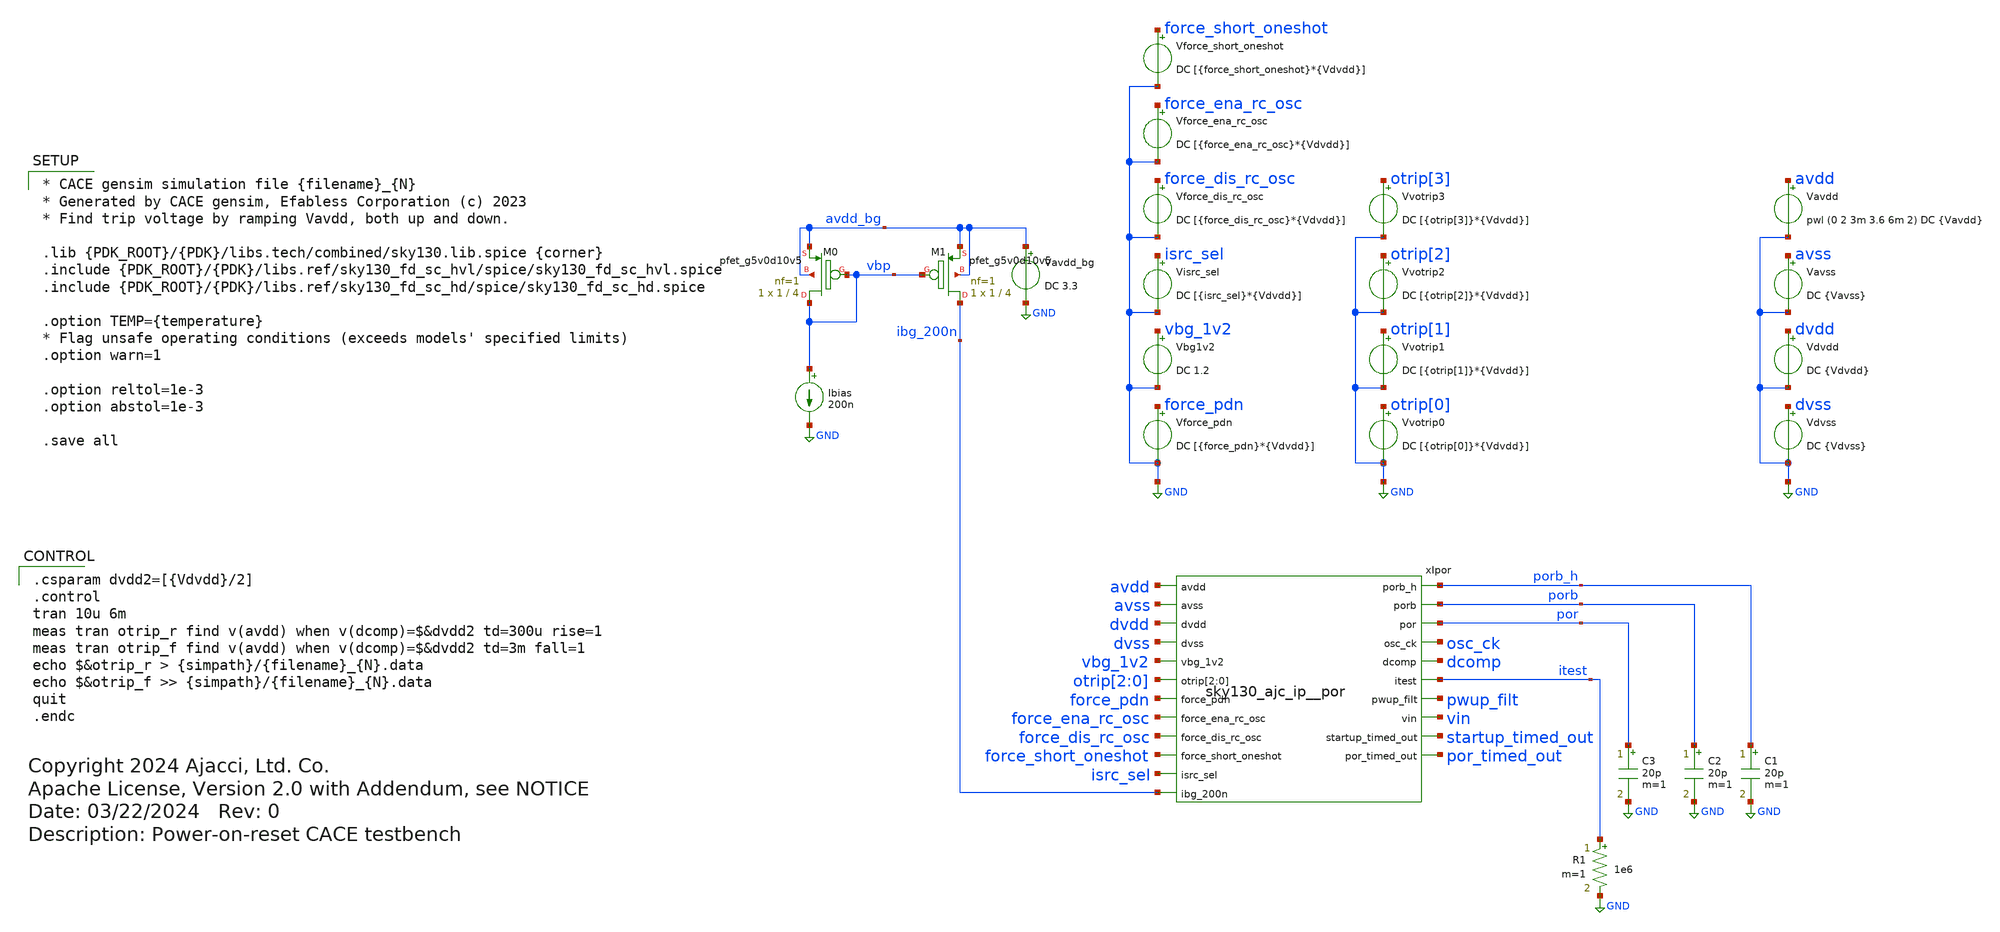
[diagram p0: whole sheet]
** sch_path: cace/trip_up_down.sch
* Copyright 2024 Ajacci, Ltd. Co.
* Apache License, Version 2.0 with Addendum, see NOTICE
**.subckt trip_up_down
Ibias vbp GND 200n
XM1 ibg_200n vbp avdd_bg avdd_bg sky130_fd_pr__pfet_g5v0d10v5 L=4 W=1 nf=1 ad='int((nf+1)/2) * W/nf * 0.29'
+ as='int((nf+2)/2) * W/nf * 0.29' pd='2*int((nf+1)/2) * (W/nf + 0.29)' ps='2*int((nf+2)/2) * (W/nf + 0.29)'
+ nrd='0.29 / W' nrs='0.29 / W' sa=0 sb=0 sd=0 mult=1 m=1
XM0 vbp vbp avdd_bg avdd_bg sky130_fd_pr__pfet_g5v0d10v5 L=4 W=1 nf=1 ad='int((nf+1)/2) * W/nf * 0.29'
+ as='int((nf+2)/2) * W/nf * 0.29' pd='2*int((nf+1)/2) * (W/nf + 0.29)' ps='2*int((nf+2)/2) * (W/nf + 0.29)'
+ nrd='0.29 / W' nrs='0.29 / W' sa=0 sb=0 sd=0 mult=1 m=1
R1 itest GND 1e6 m=1
C1 porb_h GND 20p m=1
Vavss avss GND DC {Vavss}
Vforce_pdn force_pdn GND DC [{force_pdn}*{Vdvdd}]
Vavdd avdd GND pwl (0 2 3m 3.6 6m 2) DC {Vavdd}
.save i(vavdd)
Vbg1v2 vbg_1v2 GND DC 1.2
Vdvss dvss GND DC {Vdvss}
Vdvdd dvdd GND DC {Vdvdd}
.save i(vdvdd)
Vvotrip0 otrip[0] GND DC [{otrip[0]}*{Vdvdd}]
.save i(vvotrip0)
Vvotrip1 otrip[1] GND DC [{otrip[1]}*{Vdvdd}]
.save i(vvotrip1)
Vvotrip2 otrip[2] GND DC [{otrip[2]}*{Vdvdd}]
.save i(vvotrip2)
Vvotrip3 otrip[3] GND DC [{otrip[3]}*{Vdvdd}]
.save i(vvotrip3)
Visrc_sel isrc_sel GND DC [{isrc_sel}*{Vdvdd}]
Vforce_dis_rc_osc force_dis_rc_osc GND DC [{force_dis_rc_osc}*{Vdvdd}]
Vforce_short_oneshot force_short_oneshot GND DC [{force_short_oneshot}*{Vdvdd}]
Vavdd_bg avdd_bg GND DC 3.3
Vforce_ena_rc_osc force_ena_rc_osc GND DC [{force_ena_rc_osc}*{Vdvdd}]
xIpor avdd porb_h porb avss dvdd por dvss osc_ck vbg_1v2 dcomp otrip[2] otrip[1] otrip[0] itest
+ force_pdn pwup_filt vin force_ena_rc_osc force_dis_rc_osc startup_timed_out por_timed_out force_short_oneshot
+ isrc_sel ibg_200n sky130_ajc_ip__por
C2 porb GND 20p m=1
C3 por GND 20p m=1
**** begin user architecture code

* CACE gensim simulation file {filename}_{N}
* Generated by CACE gensim, Efabless Corporation (c) 2023
* Find trip voltage by ramping Vavdd, both up and down.

.lib {PDK_ROOT}/{PDK}/libs.tech/combined/sky130.lib.spice {corner}
.include {PDK_ROOT}/{PDK}/libs.ref/sky130_fd_sc_hvl/spice/sky130_fd_sc_hvl.spice
.include {PDK_ROOT}/{PDK}/libs.ref/sky130_fd_sc_hd/spice/sky130_fd_sc_hd.spice

.option TEMP={temperature}
* Flag unsafe operating conditions (exceeds models' specified limits)
.option warn=1

.option reltol=1e-3
.option abstol=1e-3

.save all



.csparam dvdd2=[{Vdvdd}/2]
.control
tran 10u 6m
meas tran otrip_r find v(avdd) when v(dcomp)=$&dvdd2 td=300u rise=1
meas tran otrip_f find v(avdd) when v(dcomp)=$&dvdd2 td=3m fall=1
echo $&otrip_r > {simpath}/{filename}_{N}.data
echo $&otrip_f >> {simpath}/{filename}_{N}.data
quit
.endc


**** end user architecture code
**.ends
.GLOBAL GND
.end
